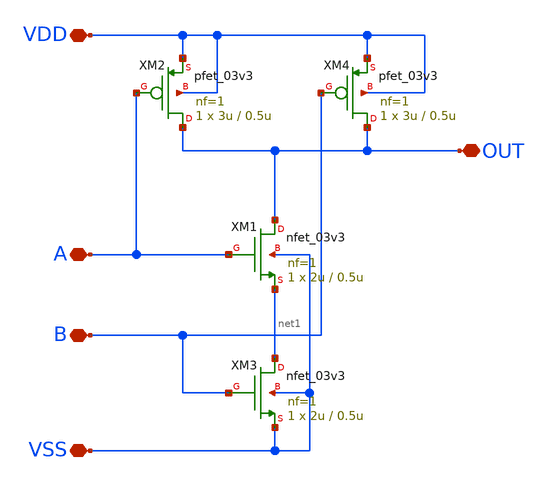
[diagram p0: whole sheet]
** sch_path: designs/libs/xp_core_analog/asc_NAND/asc_NAND.sch
**.subckt asc_NAND VDD VSS B A OUT
*.iopin VDD
*.iopin VSS
*.iopin B
*.iopin A
*.iopin OUT
XM1 OUT A net1 VSS nfet_03v3 L=0.5u W=2u nf=1 ad='int((nf+1)/2) * W/nf * 0.18u' as='int((nf+2)/2) * W/nf * 0.18u'
+ pd='2*int((nf+1)/2) * (W/nf + 0.18u)' ps='2*int((nf+2)/2) * (W/nf + 0.18u)' nrd='0.18u / W' nrs='0.18u / W'
+ sa=0 sb=0 sd=0 m=1
XM2 OUT A VDD VDD pfet_03v3 L=0.5u W=3u nf=1 ad='int((nf+1)/2) * W/nf * 0.18u' as='int((nf+2)/2) * W/nf * 0.18u'
+ pd='2*int((nf+1)/2) * (W/nf + 0.18u)' ps='2*int((nf+2)/2) * (W/nf + 0.18u)' nrd='0.18u / W' nrs='0.18u / W'
+ sa=0 sb=0 sd=0 m=1
XM3 net1 B VSS VSS nfet_03v3 L=0.5u W=2u nf=1 ad='int((nf+1)/2) * W/nf * 0.18u' as='int((nf+2)/2) * W/nf * 0.18u'
+ pd='2*int((nf+1)/2) * (W/nf + 0.18u)' ps='2*int((nf+2)/2) * (W/nf + 0.18u)' nrd='0.18u / W' nrs='0.18u / W'
+ sa=0 sb=0 sd=0 m=1
XM4 OUT B VDD VDD pfet_03v3 L=0.5u W=3u nf=1 ad='int((nf+1)/2) * W/nf * 0.18u' as='int((nf+2)/2) * W/nf * 0.18u'
+ pd='2*int((nf+1)/2) * (W/nf + 0.18u)' ps='2*int((nf+2)/2) * (W/nf + 0.18u)' nrd='0.18u / W' nrs='0.18u / W'
+ sa=0 sb=0 sd=0 m=1
**.ends
.end
